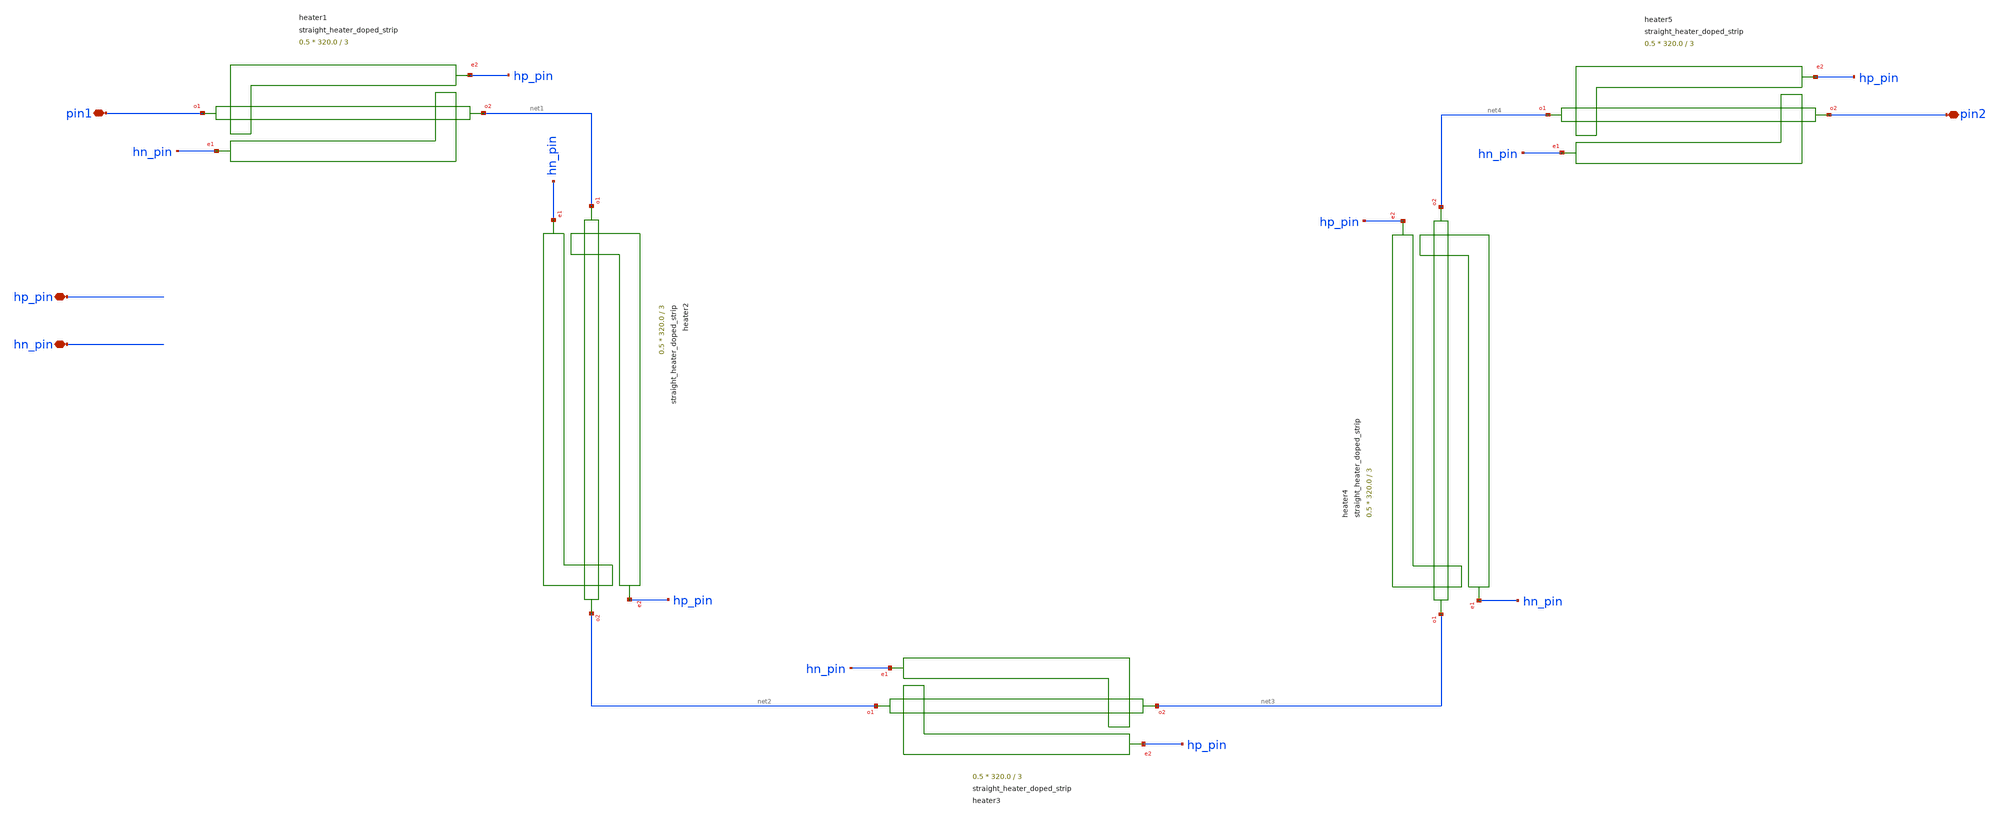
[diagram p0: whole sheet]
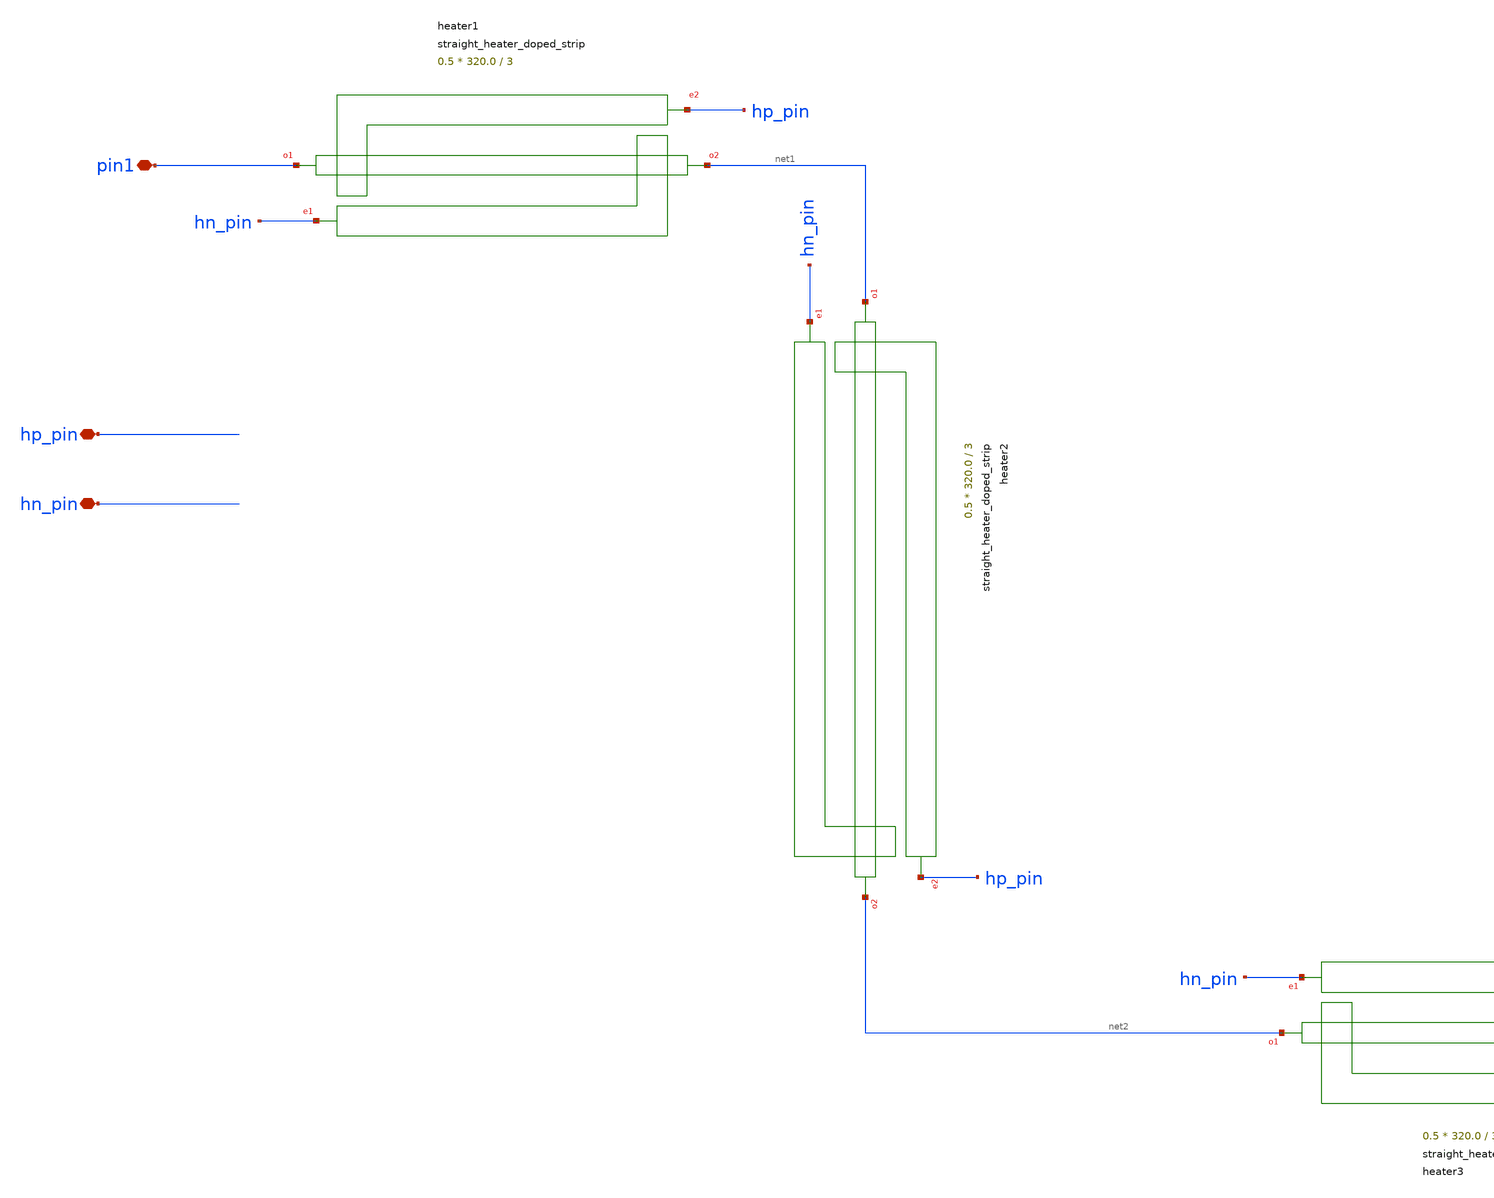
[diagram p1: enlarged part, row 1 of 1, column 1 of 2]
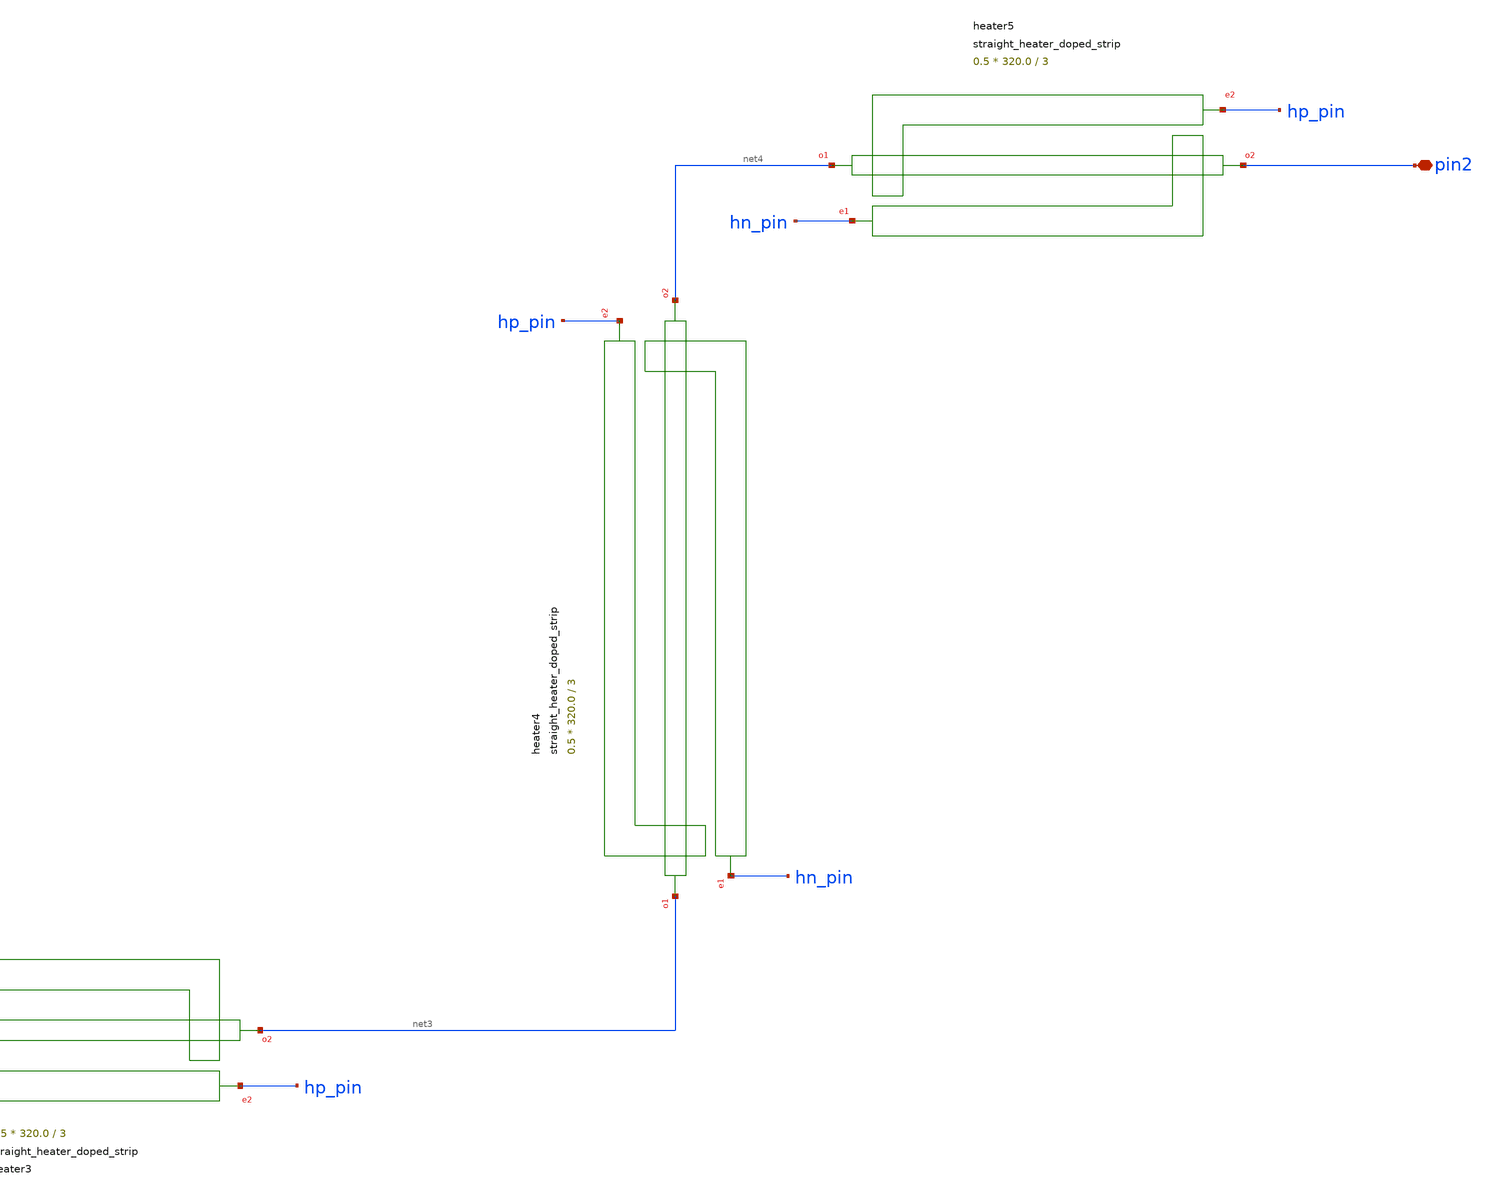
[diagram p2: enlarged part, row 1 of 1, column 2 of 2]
** sch_path: cells/xschem/tests/test_straight_heater_doped_strip.sch
* SPDX-FileCopyrightText: 2023 Mabrains Company
* Licensed under the GNU GENERAL PUBLIC License, Version 3.0 (the "License");
* you may not use this file except in compliance with the License.
* GNU GENERAL PUBLIC LICENSE
* Version 3, 29 June 2007
* This program is free software: you can redistripute it and/or modify
* it under the terms of the GNU General Public License as published
* by the Free Software Foundation, either 3 of the License, or
* (at your option) any later version.
* This program is distriputed in the hope that it will be useful,
* but WITHOUT ANY WARRANTY; without even the implied warranty of
* MERCHANTABILITY or FITNESS FOR A PARTICULAR PURPOSE.  See the
* GNU General Public License for more details.
* You should have received a copy of the GNU General Public License
* along with this program.  If not, see <https://www.gnu.org/licenses/>.
* SPDX-License-Identifier: GPL-3.0
**.subckt test_straight_heater_doped_strip pin1 pin2 hp_pin hn_pin
*.iopin pin1
*.iopin pin2
*.iopin hp_pin
*.iopin hn_pin
Pheater1 pin1 net1 hn_pin hp_pin straight_heater_doped_strip length=320.0 nsections=3
+ heater_width=2.0 heater_gap=0.8 via_stack_gap=0.0 width=0.5 xoffset_tip1=0.2 xoffset_tip2=0.4
Pheater2 net1 net2 hn_pin hp_pin straight_heater_doped_strip length=320.0 nsections=3
+ heater_width=2.0 heater_gap=0.8 via_stack_gap=0.0 width=0.5 xoffset_tip1=0.2 xoffset_tip2=0.4
Pheater3 net2 net3 hn_pin hp_pin straight_heater_doped_strip length=320.0 nsections=3
+ heater_width=2.0 heater_gap=0.8 via_stack_gap=0.0 width=0.5 xoffset_tip1=0.2 xoffset_tip2=0.4
Pheater4 net3 net4 hn_pin hp_pin straight_heater_doped_strip length=320.0 nsections=3
+ heater_width=2.0 heater_gap=0.8 via_stack_gap=0.0 width=0.5 xoffset_tip1=0.2 xoffset_tip2=0.4
Pheater5 net4 pin2 hn_pin hp_pin straight_heater_doped_strip length=320.0 nsections=3
+ heater_width=2.0 heater_gap=0.8 via_stack_gap=0.0 width=0.5 xoffset_tip1=0.2 xoffset_tip2=0.4
**.ends
.end
